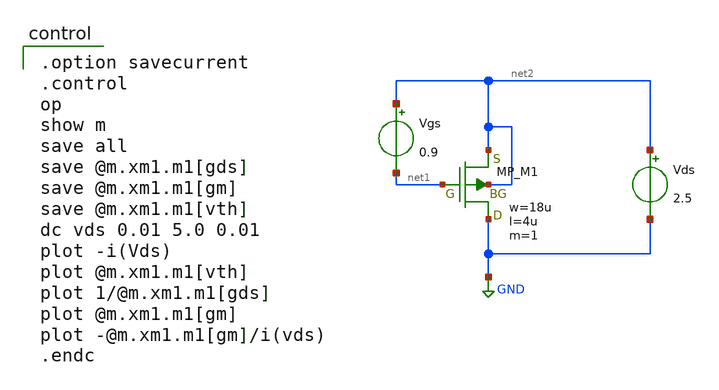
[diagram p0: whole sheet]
** sch_path: member_project/opamp/july_fifth/pfet_idvds.sch
**.subckt pfet_idvds
Vgs net2 net1 0.9
Vds net2 GND 2.5
XM1 GND net1 net2 net2 PMOS w=18u l=4u as=0 ad=0 ps=0 pd=0 nrd=0 nrs=0 m=1
**** begin user architecture code

.option savecurrent
.control
op
show m
save all
save @m.xm1.m1[gds]
save @m.xm1.m1[gm]
save @m.xm1.m1[vth]
dc vds 0.01 5.0 0.01
plot -i(Vds)
plot @m.xm1.m1[vth]
plot 1/@m.xm1.m1[gds]
plot @m.xm1.m1[gm]
plot -@m.xm1.m1[gm]/i(vds)
.endc

 .include $::LIB/ip62_models
**** end user architecture code
**.ends
.GLOBAL GND
.end
